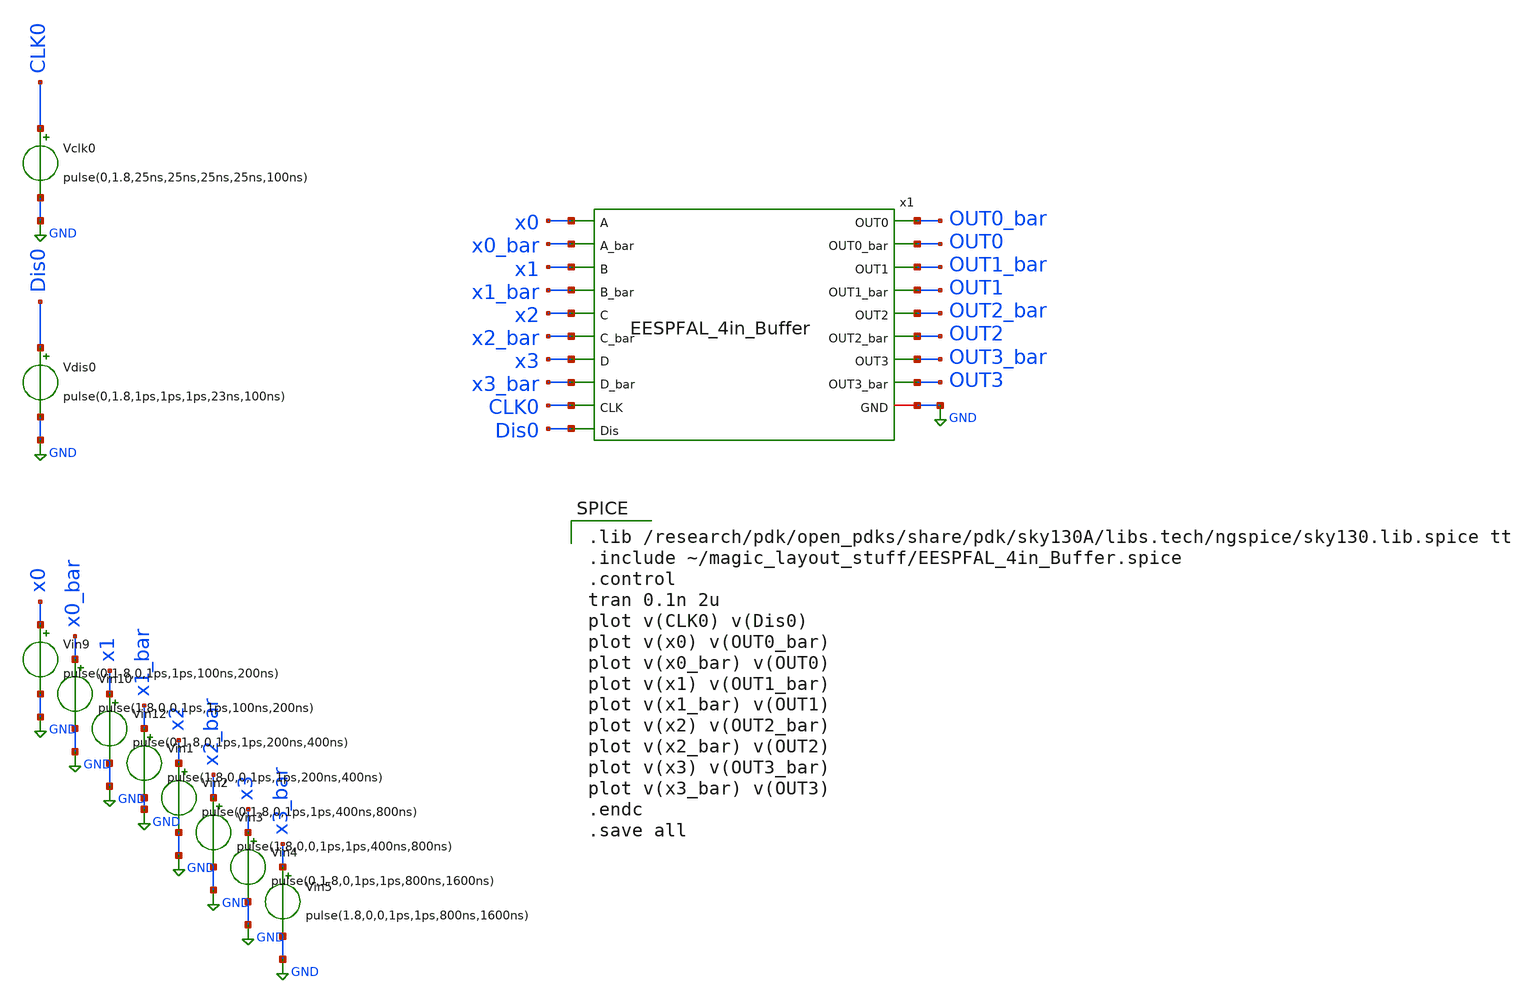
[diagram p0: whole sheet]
** sch_path: skywater_stuff/EESPFAL_4in_Buffer_sim.sch
**.subckt EESPFAL_4in_Buffer_sim
Vdis0 Dis0 GND pulse(0,1.8,1ps,1ps,1ps,23ns,100ns)
Vclk0 CLK0 GND pulse(0,1.8,25ns,25ns,25ns,25ns,100ns)
x1 x0 x0_bar x1 x1_bar x2 x2_bar x3 x3_bar OUT0_bar OUT0 OUT1_bar OUT1 OUT2_bar OUT2 OUT3_bar OUT3
+ Dis0 GND CLK0 EESPFAL_4in_Buffer
Vin9 x0 GND pulse(0,1.8,0,1ps,1ps,100ns,200ns)
Vin10 x0_bar GND pulse(1.8,0,0,1ps,1ps,100ns,200ns)
Vin12 x1 GND pulse(0,1.8,0,1ps,1ps,200ns,400ns)
Vin1 x1_bar GND pulse(1.8,0,0,1ps,1ps,200ns,400ns)
Vin2 x2 GND pulse(0,1.8,0,1ps,1ps,400ns,800ns)
Vin3 x2_bar GND pulse(1.8,0,0,1ps,1ps,400ns,800ns)
Vin4 x3 GND pulse(0,1.8,0,1ps,1ps,800ns,1600ns)
Vin5 x3_bar GND pulse(1.8,0,0,1ps,1ps,800ns,1600ns)
**** begin user architecture code

.lib /research/pdk/open_pdks/share/pdk/sky130A/libs.tech/ngspice/sky130.lib.spice tt
.include ~/magic_layout_stuff/EESPFAL_4in_Buffer.spice
.control
tran 0.1n 2u
plot v(CLK0) v(Dis0)
plot v(x0) v(OUT0_bar)
plot v(x0_bar) v(OUT0)
plot v(x1) v(OUT1_bar)
plot v(x1_bar) v(OUT1)
plot v(x2) v(OUT2_bar)
plot v(x2_bar) v(OUT2)
plot v(x3) v(OUT3_bar)
plot v(x3_bar) v(OUT3)
.endc
.save all

**** end user architecture code
**.ends
.GLOBAL GND
.end
